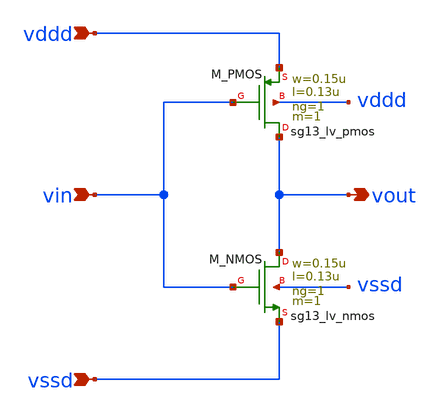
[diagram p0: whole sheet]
** sch_path: Inverter_testcase/inverter.sch
**.subckt inverter vddd vssd vin vout
*.ipin vddd
*.ipin vssd
*.ipin vin
*.opin vout
XM_PMOS vout vin vddd vddd sg13_lv_pmos w=0.15u l=0.13u ng=1 m=1 mm_ok=1
XM_NMOS vout vin vssd vssd sg13_lv_nmos w=0.15u l=0.13u ng=1 m=1 mm_ok=1
**.ends
.end
